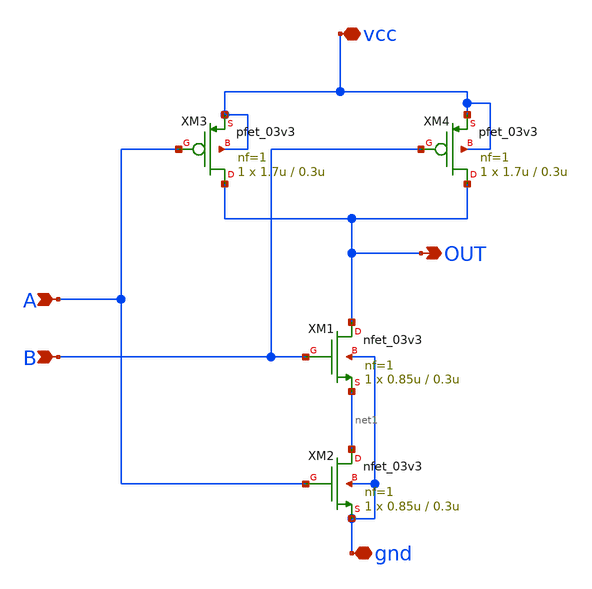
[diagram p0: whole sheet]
** sch_path: designs/libs/core_digital/mux2x1_nand/nand.sch
**.subckt nand A B OUT vcc gnd
*.ipin A
*.ipin B
*.opin OUT
*.iopin vcc
*.iopin gnd
XM1 OUT B net1 gnd nfet_03v3 L=0.3u W=0.85u nf=1 ad='int((nf+1)/2) * W/nf * 0.18u' as='int((nf+2)/2) * W/nf * 0.18u'
+ pd='2*int((nf+1)/2) * (W/nf + 0.18u)' ps='2*int((nf+2)/2) * (W/nf + 0.18u)' nrd='0.18u / W' nrs='0.18u / W'
+ sa=0 sb=0 sd=0 m=1
XM2 net1 A gnd gnd nfet_03v3 L=0.3u W=0.85u nf=1 ad='int((nf+1)/2) * W/nf * 0.18u' as='int((nf+2)/2) * W/nf * 0.18u'
+ pd='2*int((nf+1)/2) * (W/nf + 0.18u)' ps='2*int((nf+2)/2) * (W/nf + 0.18u)' nrd='0.18u / W' nrs='0.18u / W'
+ sa=0 sb=0 sd=0 m=1
XM3 OUT A vcc vcc pfet_03v3 L=0.3u W=1.7u nf=1 ad='int((nf+1)/2) * W/nf * 0.18u' as='int((nf+2)/2) * W/nf * 0.18u'
+ pd='2*int((nf+1)/2) * (W/nf + 0.18u)' ps='2*int((nf+2)/2) * (W/nf + 0.18u)' nrd='0.18u / W' nrs='0.18u / W'
+ sa=0 sb=0 sd=0 m=1
XM4 OUT B vcc vcc pfet_03v3 L=0.3u W=1.7u nf=1 ad='int((nf+1)/2) * W/nf * 0.18u' as='int((nf+2)/2) * W/nf * 0.18u'
+ pd='2*int((nf+1)/2) * (W/nf + 0.18u)' ps='2*int((nf+2)/2) * (W/nf + 0.18u)' nrd='0.18u / W' nrs='0.18u / W'
+ sa=0 sb=0 sd=0 m=1
**.ends
.end
